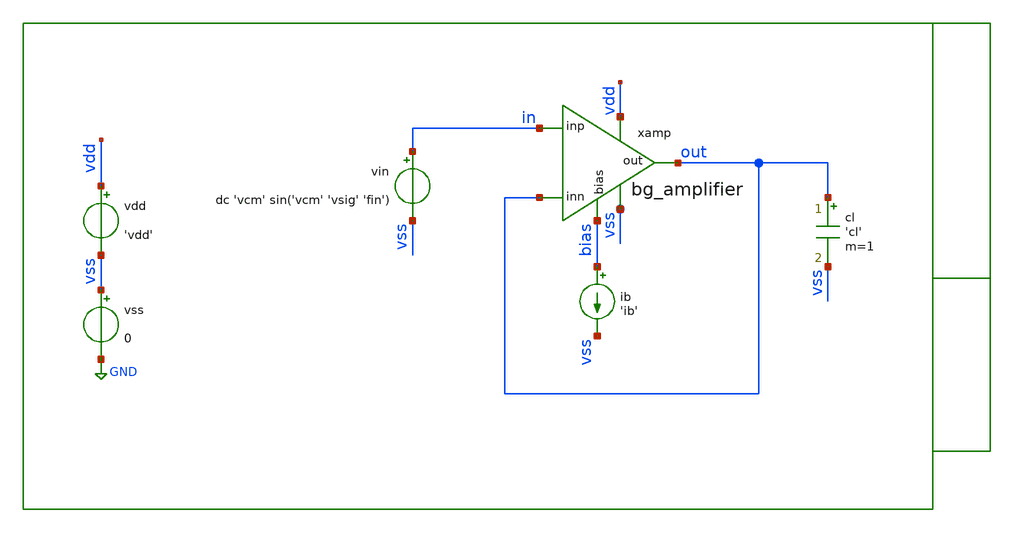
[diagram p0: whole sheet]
** sch_path: xschem/tb/bandgap_cm/bg_amplifier/tr_bg_amplifier.sch
**.subckt tr_bg_amplifier
vin in vss dc 'vcm' sin('vcm' 'vsig' 'fin')
cl out vss 'cl' m=1
vdd vdd vss 'vdd'
vss vss GND 0
xamp vdd out in out vss bias bg_amplifier
ib bias vss 'ib'
**** begin user architecture code
 * control

.param vdd=3.3
.param vcm='vdd/2'
.param ib=1u
.param cl=1p
.param fin=1e3
.param vsig='vdd/2'

.control

save all
tran 1u 1m
gnuplot p1 in out
set wr_singlescale
set wr_vecnames
wrdata output.csv in out
.endc

 * Model Corners

.include $::CORNERS/ngspice/tt.spice
*.include $::CORNERS/ngspice/ff.spice
*.include $::CORNERS/ngspice/ss.spice
*.include $::CORNERS/ngspice/sf.spice
*.include $::CORNERS/ngspice/fs.spice

 * extract

* pex
*.include $::DESIGN_PATH/sch/bandgap_cm/bg_amplifier/bg_amplifier.pex.spice

**** end user architecture code
**.ends

* expanding   symbol:  sch/bandgap_cm/bg_amplifier/bg_amplifier.sym # of pins=6
** sym_path: xschem/sch/bandgap_cm/bg_amplifier/bg_amplifier.sym
** sch_path: xschem/sch/bandgap_cm/bg_amplifier/bg_amplifier.sch
.subckt bg_amplifier vdd out inp inn vss bias
*.ipin inn
*.ipin inp
*.opin out
*.iopin bias
*.iopin vdd
*.iopin vss
XMB5 vbn1 vbn1 vss vss nfet_06v0 L=2u W=16u nf=2 ad='int((nf+1)/2) * W/nf * 0.18u' as='int((nf+2)/2) * W/nf * 0.18u'
+ pd='2*int((nf+1)/2) * (W/nf + 0.18u)' ps='2*int((nf+2)/2) * (W/nf + 0.18u)' nrd='0.18u / W' nrs='0.18u / W'
+ sa=0 sb=0 sd=0 m=4 par=4
XMC1 von vbn1 vss vss nfet_06v0 L=2u W=16u nf=2 ad='int((nf+1)/2) * W/nf * 0.18u' as='int((nf+2)/2) * W/nf * 0.18u'
+ pd='2*int((nf+1)/2) * (W/nf + 0.18u)' ps='2*int((nf+2)/2) * (W/nf + 0.18u)' nrd='0.18u / W' nrs='0.18u / W'
+ sa=0 sb=0 sd=0 m=10 par=10
XMC2 vop vbn1 vss vss nfet_06v0 L=2u W=16u nf=2 ad='int((nf+1)/2) * W/nf * 0.18u' as='int((nf+2)/2) * W/nf * 0.18u'
+ pd='2*int((nf+1)/2) * (W/nf + 0.18u)' ps='2*int((nf+2)/2) * (W/nf + 0.18u)' nrd='0.18u / W' nrs='0.18u / W'
+ sa=0 sb=0 sd=0 m=10 par=10
XMC3 mirr vbn2 von vss nfet_06v0 L=2u W=16u nf=2 ad='int((nf+1)/2) * W/nf * 0.18u' as='int((nf+2)/2) * W/nf * 0.18u'
+ pd='2*int((nf+1)/2) * (W/nf + 0.18u)' ps='2*int((nf+2)/2) * (W/nf + 0.18u)' nrd='0.18u / W' nrs='0.18u / W'
+ sa=0 sb=0 sd=0 m=4 par=4
XMC4 out vbn2 vop vss nfet_06v0 L=2u W=16u nf=2 ad='int((nf+1)/2) * W/nf * 0.18u' as='int((nf+2)/2) * W/nf * 0.18u'
+ pd='2*int((nf+1)/2) * (W/nf + 0.18u)' ps='2*int((nf+2)/2) * (W/nf + 0.18u)' nrd='0.18u / W' nrs='0.18u / W'
+ sa=0 sb=0 sd=0 m=4 par=4
XMB3 bias bias vbp1 vdd pfet_06v0 L=2u W=16u nf=2 ad='int((nf+1)/2) * W/nf * 0.18u' as='int((nf+2)/2) * W/nf * 0.18u'
+ pd='2*int((nf+1)/2) * (W/nf + 0.18u)' ps='2*int((nf+2)/2) * (W/nf + 0.18u)' nrd='0.18u / W' nrs='0.18u / W'
+ sa=0 sb=0 sd=0 m=2 par=2
XMB1 vbp1 vbp1 vdd vdd pfet_06v0 L=2u W=16u nf=2 ad='int((nf+1)/2) * W/nf * 0.18u' as='int((nf+2)/2) * W/nf * 0.18u'
+ pd='2*int((nf+1)/2) * (W/nf + 0.18u)' ps='2*int((nf+2)/2) * (W/nf + 0.18u)' nrd='0.18u / W' nrs='0.18u / W'
+ sa=0 sb=0 sd=0 m=4 par=4
XMB2 vbn2 vbp1 vdd vdd pfet_06v0 L=2u W=16u nf=2 ad='int((nf+1)/2) * W/nf * 0.18u' as='int((nf+2)/2) * W/nf * 0.18u'
+ pd='2*int((nf+1)/2) * (W/nf + 0.18u)' ps='2*int((nf+2)/2) * (W/nf + 0.18u)' nrd='0.18u / W' nrs='0.18u / W'
+ sa=0 sb=0 sd=0 m=4 par=4
XMT1 vcm vbp1 vdd vdd pfet_06v0 L=2u W=16u nf=2 ad='int((nf+1)/2) * W/nf * 0.18u' as='int((nf+2)/2) * W/nf * 0.18u'
+ pd='2*int((nf+1)/2) * (W/nf + 0.18u)' ps='2*int((nf+2)/2) * (W/nf + 0.18u)' nrd='0.18u / W' nrs='0.18u / W'
+ sa=0 sb=0 sd=0 m=8 par=8
XMD1 von inp vcm vdd pfet_06v0 L=4u W=16u nf=2 ad='int((nf+1)/2) * W/nf * 0.18u' as='int((nf+2)/2) * W/nf * 0.18u'
+ pd='2*int((nf+1)/2) * (W/nf + 0.18u)' ps='2*int((nf+2)/2) * (W/nf + 0.18u)' nrd='0.18u / W' nrs='0.18u / W'
+ sa=0 sb=0 sd=0 m=4 par=4
XMD2 vop inn vcm vdd pfet_06v0 L=4u W=16u nf=2 ad='int((nf+1)/2) * W/nf * 0.18u' as='int((nf+2)/2) * W/nf * 0.18u'
+ pd='2*int((nf+1)/2) * (W/nf + 0.18u)' ps='2*int((nf+2)/2) * (W/nf + 0.18u)' nrd='0.18u / W' nrs='0.18u / W'
+ sa=0 sb=0 sd=0 m=4 par=4
XMC7 vda mirr vdd vdd pfet_06v0 L=2u W=16u nf=2 ad='int((nf+1)/2) * W/nf * 0.18u' as='int((nf+2)/2) * W/nf * 0.18u'
+ pd='2*int((nf+1)/2) * (W/nf + 0.18u)' ps='2*int((nf+2)/2) * (W/nf + 0.18u)' nrd='0.18u / W' nrs='0.18u / W'
+ sa=0 sb=0 sd=0 m=2 par=2
XMC8 vdb mirr vdd vdd pfet_06v0 L=2u W=16u nf=2 ad='int((nf+1)/2) * W/nf * 0.18u' as='int((nf+2)/2) * W/nf * 0.18u'
+ pd='2*int((nf+1)/2) * (W/nf + 0.18u)' ps='2*int((nf+2)/2) * (W/nf + 0.18u)' nrd='0.18u / W' nrs='0.18u / W'
+ sa=0 sb=0 sd=0 m=2 par=2
XMC5 mirr bias vda vdd pfet_06v0 L=2u W=16u nf=2 ad='int((nf+1)/2) * W/nf * 0.18u' as='int((nf+2)/2) * W/nf * 0.18u'
+ pd='2*int((nf+1)/2) * (W/nf + 0.18u)' ps='2*int((nf+2)/2) * (W/nf + 0.18u)' nrd='0.18u / W' nrs='0.18u / W'
+ sa=0 sb=0 sd=0 m=4 par=4
XMC6 out bias vdb vdd pfet_06v0 L=2u W=16u nf=2 ad='int((nf+1)/2) * W/nf * 0.18u' as='int((nf+2)/2) * W/nf * 0.18u'
+ pd='2*int((nf+1)/2) * (W/nf + 0.18u)' ps='2*int((nf+2)/2) * (W/nf + 0.18u)' nrd='0.18u / W' nrs='0.18u / W'
+ sa=0 sb=0 sd=0 m=4 par=4
XMB4 vbn2 vbn2 vbn1 vss nfet_06v0 L=2u W=16u nf=2 ad='int((nf+1)/2) * W/nf * 0.18u' as='int((nf+2)/2) * W/nf * 0.18u'
+ pd='2*int((nf+1)/2) * (W/nf + 0.18u)' ps='2*int((nf+2)/2) * (W/nf + 0.18u)' nrd='0.18u / W' nrs='0.18u / W'
+ sa=0 sb=0 sd=0 m=4 par=4
XMDUM1 vdd vdd vdd vdd pfet_06v0 L=2u W=16u nf=2 ad='int((nf+1)/2) * W/nf * 0.18u' as='int((nf+2)/2) * W/nf * 0.18u'
+ pd='2*int((nf+1)/2) * (W/nf + 0.18u)' ps='2*int((nf+2)/2) * (W/nf + 0.18u)' nrd='0.18u / W' nrs='0.18u / W'
+ sa=0 sb=0 sd=0 m=4 par=4
XMDUM2 vdd vdd vdd vdd pfet_06v0 L=2u W=16u nf=2 ad='int((nf+1)/2) * W/nf * 0.18u' as='int((nf+2)/2) * W/nf * 0.18u'
+ pd='2*int((nf+1)/2) * (W/nf + 0.18u)' ps='2*int((nf+2)/2) * (W/nf + 0.18u)' nrd='0.18u / W' nrs='0.18u / W'
+ sa=0 sb=0 sd=0 m=4 par=4
XMDUM3 vdd vdd vdd vdd pfet_06v0 L=2u W=16u nf=2 ad='int((nf+1)/2) * W/nf * 0.18u' as='int((nf+2)/2) * W/nf * 0.18u'
+ pd='2*int((nf+1)/2) * (W/nf + 0.18u)' ps='2*int((nf+2)/2) * (W/nf + 0.18u)' nrd='0.18u / W' nrs='0.18u / W'
+ sa=0 sb=0 sd=0 m=2 par=2
XMDUM4 vss vss vss vss nfet_06v0 L=2u W=16u nf=2 ad='int((nf+1)/2) * W/nf * 0.18u' as='int((nf+2)/2) * W/nf * 0.18u'
+ pd='2*int((nf+1)/2) * (W/nf + 0.18u)' ps='2*int((nf+2)/2) * (W/nf + 0.18u)' nrd='0.18u / W' nrs='0.18u / W'
+ sa=0 sb=0 sd=0 m=2 par=2
XMDUM5 vss vss vss vss nfet_06v0 L=2u W=16u nf=2 ad='int((nf+1)/2) * W/nf * 0.18u' as='int((nf+2)/2) * W/nf * 0.18u'
+ pd='2*int((nf+1)/2) * (W/nf + 0.18u)' ps='2*int((nf+2)/2) * (W/nf + 0.18u)' nrd='0.18u / W' nrs='0.18u / W'
+ sa=0 sb=0 sd=0 m=2 par=2
XMDUM6 vdd vdd vdd vdd pfet_06v0 L=4u W=16u nf=2 ad='int((nf+1)/2) * W/nf * 0.18u' as='int((nf+2)/2) * W/nf * 0.18u'
+ pd='2*int((nf+1)/2) * (W/nf + 0.18u)' ps='2*int((nf+2)/2) * (W/nf + 0.18u)' nrd='0.18u / W' nrs='0.18u / W'
+ sa=0 sb=0 sd=0 m=16 par=16
.ends

.GLOBAL GND
.end
